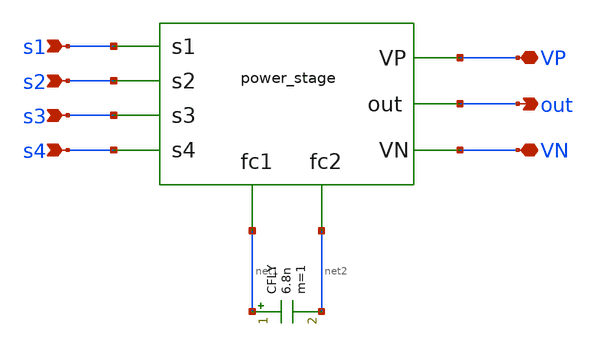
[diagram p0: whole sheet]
** sch_path: xschem/release/converter.sch
**.subckt converter s1 s2 s3 s4 VP VN out
*.ipin s1
*.ipin s2
*.ipin s3
*.ipin s4
*.iopin VP
*.iopin VN
*.opin out
X1 s1 s2 s3 s4 net1 net2 out VP VN power_stage
CFLY net1 net2 6.8n m=1
**.ends

* expanding   symbol:  power_stage.sym # of pins=9
** sym_path: xschem/release/power_stage.sym
** sch_path: xschem/release/power_stage.sch
.subckt power_stage s1 s2 s3 s4 fc1 fc2 out VP VN
*.ipin s1
*.ipin s2
*.ipin s3
*.ipin s4
*.iopin VP
*.iopin VN
*.opin out
*.opin fc1
*.opin fc2
XM3 out s3 fc2 fc2 sky130_fd_pr__nfet_g5v0d10v5 L=0.5 W=4.38 nf=1 ad='int((nf+1)/2) * W/nf * 0.29' as='int((nf+2)/2) * W/nf * 0.29'
+ pd='2*int((nf+1)/2) * (W/nf + 0.29)' ps='2*int((nf+2)/2) * (W/nf + 0.29)' nrd='0.29 / W' nrs='0.29 / W'
+ sa=0 sb=0 sd=0 mult=2520 m=2520
XM2 out s2 fc1 fc1 sky130_fd_pr__pfet_g5v0d10v5 L=0.5 W=4.38 nf=1 ad='int((nf+1)/2) * W/nf * 0.29' as='int((nf+2)/2) * W/nf * 0.29'
+ pd='2*int((nf+1)/2) * (W/nf + 0.29)' ps='2*int((nf+2)/2) * (W/nf + 0.29)' nrd='0.29 / W' nrs='0.29 / W'
+ sa=0 sb=0 sd=0 mult=4506 m=4506
XM1 fc1 s1 VP VP sky130_fd_pr__pfet_g5v0d10v5 L=0.5 W=4.38 nf=1 ad='int((nf+1)/2) * W/nf * 0.29' as='int((nf+2)/2) * W/nf * 0.29'
+ pd='2*int((nf+1)/2) * (W/nf + 0.29)' ps='2*int((nf+2)/2) * (W/nf + 0.29)' nrd='0.29 / W' nrs='0.29 / W'
+ sa=0 sb=0 sd=0 mult=4506 m=4506
XM4 fc2 s4 VN VN sky130_fd_pr__nfet_g5v0d10v5 L=0.5 W=4.38 nf=1 ad='int((nf+1)/2) * W/nf * 0.29' as='int((nf+2)/2) * W/nf * 0.29'
+ pd='2*int((nf+1)/2) * (W/nf + 0.29)' ps='2*int((nf+2)/2) * (W/nf + 0.29)' nrd='0.29 / W' nrs='0.29 / W'
+ sa=0 sb=0 sd=0 mult=2520 m=2520
.ends

.end
